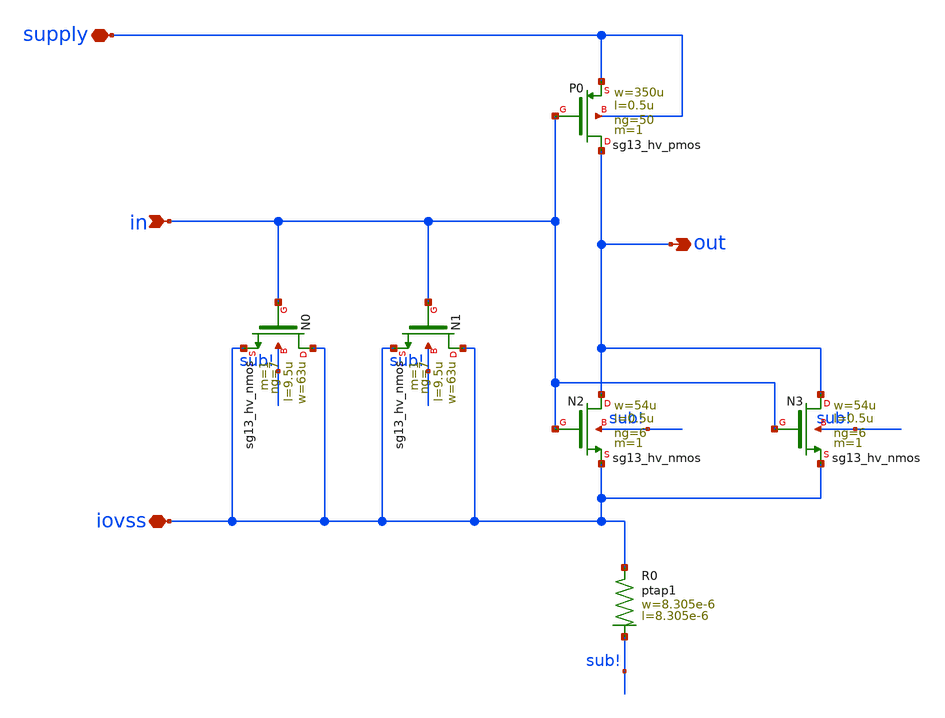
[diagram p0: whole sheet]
** sch_path: ihp-sg13g2/libs.ref/sg13g2_io/sch/xschem/sg13g2_RCClampInverter.sch
**.subckt sg13g2_RCClampInverter in out supply iovss
*.ipin in
*.opin out
*.iopin supply
*.iopin iovss
XN0 iovss in iovss sub! sg13_hv_nmos w=63u l=9.5u ng=7 m=1 mm_ok=1
XN1 iovss in iovss sub! sg13_hv_nmos w=63u l=9.5u ng=7 m=1 mm_ok=1
XN2 out in iovss sub! sg13_hv_nmos w=54u l=0.5u ng=6 m=1 mm_ok=1
XN3 out in iovss sub! sg13_hv_nmos w=54u l=0.5u ng=6 m=1 mm_ok=1
XP0 out in supply supply sg13_hv_pmos w=350u l=0.5u ng=50 m=1 mm_ok=1
XR0 iovss sub! ptap1 R=9.59 w=8.305e-6 l=8.305e-6
**.ends
.end
